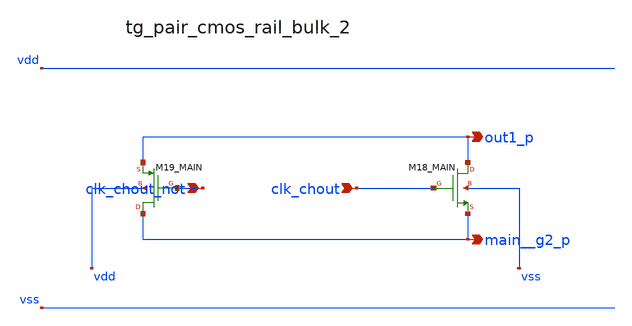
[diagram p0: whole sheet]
** sch_path: analog-db/raw/ia_004_fan_chopper_rrl/hier/blocks/tg_pair_cmos_rail_bulk_2.sch
**.subckt tg_pair_cmos_rail_bulk_2 clk_chout_not clk_chout out1_p main__g2_p
*.ipin clk_chout_not
*.ipin clk_chout
*.opin out1_p
*.opin main__g2_p
XM18_MAIN out1_p clk_chout main__g2_p vss sg13_lv_nmos w=x_dut_xm18_main_w l=x_dut_xm18_main_l ng=1
+ m=x_dut_xm18_main_m
XM19_MAIN main__g2_p clk_chout_not out1_p vdd sg13_lv_pmos w=x_dut_xm19_main_w l=x_dut_xm19_main_l
+ ng=1 m=x_dut_xm19_main_m
**.ends
.end
